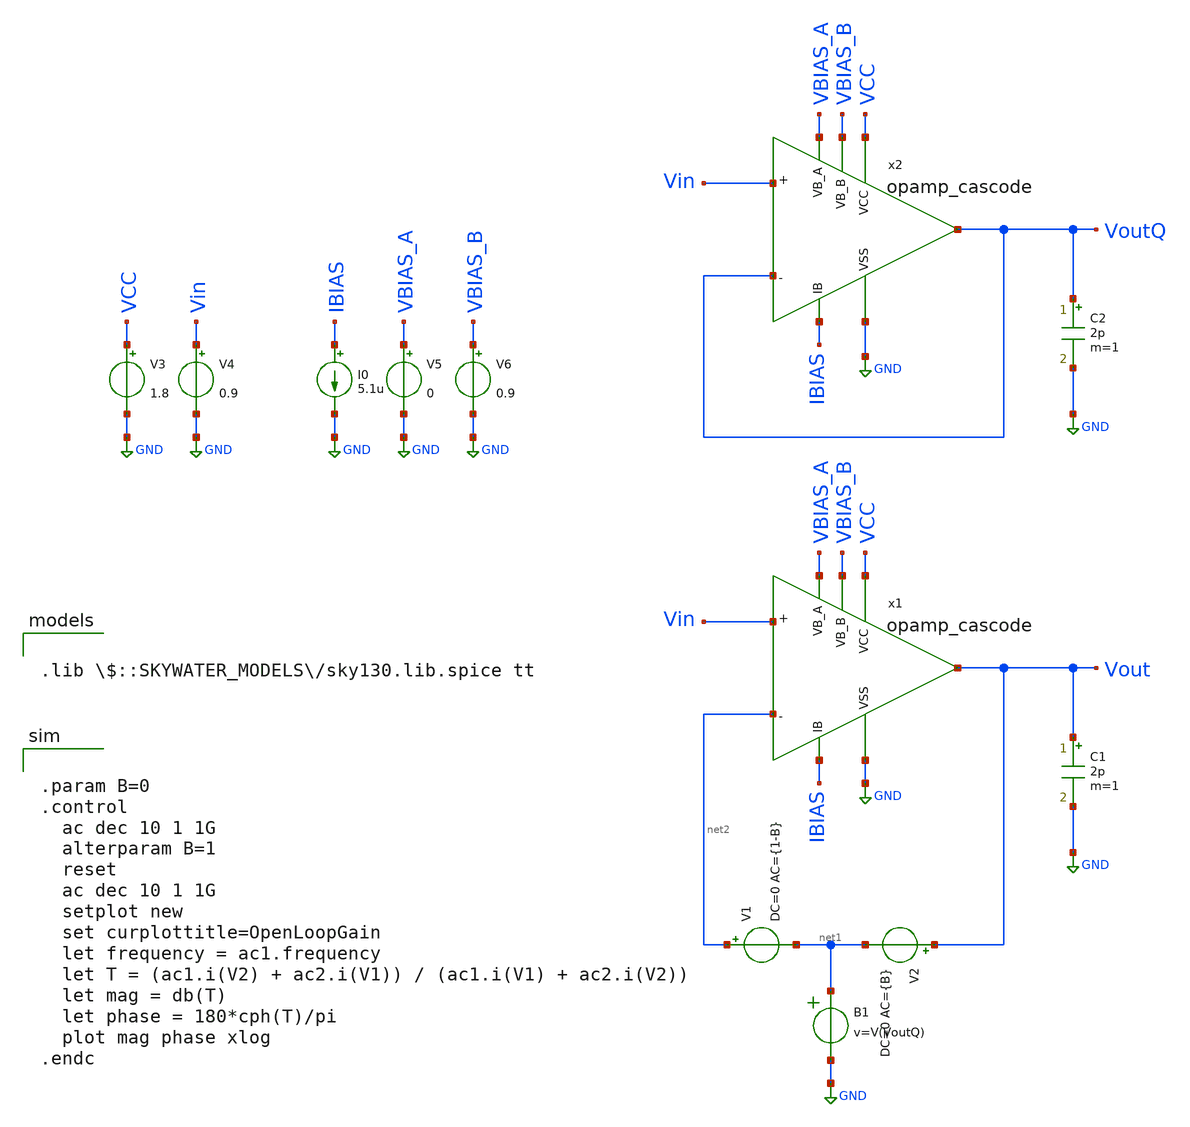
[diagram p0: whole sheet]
** sch_path: opamp_cascode_ac_ochoa.sch
**.subckt opamp_cascode_ac_ochoa
V3 VCC GND 1.8
V4 Vin GND 0.9
V2 Vout net1 DC=0 AC={B}
C1 Vout GND 2p m=1
C2 VoutQ GND 2p m=1
V1 net2 net1 DC=0 AC={1-B}
B1 net1 GND v=V(VoutQ)
V5 VBIAS_A GND 0
V6 VBIAS_B GND 0.9
I0 IBIAS GND 5.1u
x1 VCC GND VBIAS_B Vin net2 Vout IBIAS VBIAS_A opamp_cascode
x2 VCC GND VBIAS_B Vin VoutQ VoutQ IBIAS VBIAS_A opamp_cascode
**** begin user architecture code


.param B=0
.control
  ac dec 10 1 1G
  alterparam B=1
  reset
  ac dec 10 1 1G
  setplot new
  set curplottitle=OpenLoopGain
  let frequency = ac1.frequency
  let T = (ac1.i(V2) + ac2.i(V1)) / (ac1.i(V1) + ac2.i(V2))
  let mag = db(T)
  let phase = 180*cph(T)/pi
  plot mag phase xlog
.endc



.lib $::SKYWATER_MODELS/sky130.lib.spice tt

**** end user architecture code
**.ends

* expanding   symbol:  /home/zwierzak/projects/SKY130_OpAmp_GIT/opamp_cascode.sym # of pins=8
** sym_path: 03_Layout/opamp_cascode.sym
** sch_path: 03_Layout/opamp_cascode.sch
.subckt opamp_cascode VCC VSS VB_B IN_P IN_M OUT IB VB_A
*.ipin IN_P
*.ipin IN_M
*.ipin VCC
*.ipin VSS
*.opin OUT
*.ipin VB_A
*.ipin VB_B
*.ipin IB
XM100_3 IB IB VCC VCC sky130_fd_pr__pfet_01v8 L=3 W=5 nf=1 ad='int((nf+1)/2) * W/nf * 0.29' as='int((nf+2)/2) * W/nf * 0.29'
+ pd='2*int((nf+1)/2) * (W/nf + 0.29)' ps='2*int((nf+2)/2) * (W/nf + 0.29)' nrd='0.29 / W' nrs='0.29 / W'
+ sa=0 sb=0 sd=0 mult=2 m=2
XM10 OUT VB_A m9m10 VCC sky130_fd_pr__pfet_01v8 L=5 W=5 nf=1 ad='int((nf+1)/2) * W/nf * 0.29' as='int((nf+2)/2) * W/nf * 0.29'
+ pd='2*int((nf+1)/2) * (W/nf + 0.29)' ps='2*int((nf+2)/2) * (W/nf + 0.29)' nrd='0.29 / W' nrs='0.29 / W'
+ sa=0 sb=0 sd=0 mult=15 m=15
XM2 bias1 VB_A m1m2 VCC sky130_fd_pr__pfet_01v8 L=5 W=5 nf=1 ad='int((nf+1)/2) * W/nf * 0.29' as='int((nf+2)/2) * W/nf * 0.29'
+ pd='2*int((nf+1)/2) * (W/nf + 0.29)' ps='2*int((nf+2)/2) * (W/nf + 0.29)' nrd='0.29 / W' nrs='0.29 / W'
+ sa=0 sb=0 sd=0 mult=15 m=15
XM5 bias3 IN_M m100m5 VCC sky130_fd_pr__pfet_01v8 L=0.18 W=5 nf=1 ad='int((nf+1)/2) * W/nf * 0.29' as='int((nf+2)/2) * W/nf * 0.29'
+ pd='2*int((nf+1)/2) * (W/nf + 0.29)' ps='2*int((nf+2)/2) * (W/nf + 0.29)' nrd='0.29 / W' nrs='0.29 / W'
+ sa=0 sb=0 sd=0 mult=15 m=15
XM7 bias21 IN_P m100m5 VCC sky130_fd_pr__pfet_01v8 L=0.18 W=5 nf=1 ad='int((nf+1)/2) * W/nf * 0.29' as='int((nf+2)/2) * W/nf * 0.29'
+ pd='2*int((nf+1)/2) * (W/nf + 0.29)' ps='2*int((nf+2)/2) * (W/nf + 0.29)' nrd='0.29 / W' nrs='0.29 / W'
+ sa=0 sb=0 sd=0 mult=15 m=15
XM6 bias3 bias3 VSS VSS sky130_fd_pr__nfet_01v8 L=1 W=1.25 nf=1 ad='int((nf+1)/2) * W/nf * 0.29' as='int((nf+2)/2) * W/nf * 0.29'
+ pd='2*int((nf+1)/2) * (W/nf + 0.29)' ps='2*int((nf+2)/2) * (W/nf + 0.29)' nrd='0.29 / W' nrs='0.29 / W'
+ sa=0 sb=0 sd=0 mult=1 m=1
XM8 bias21 bias21 VSS VSS sky130_fd_pr__nfet_01v8 L=1 W=1.25 nf=1 ad='int((nf+1)/2) * W/nf * 0.29' as='int((nf+2)/2) * W/nf * 0.29'
+ pd='2*int((nf+1)/2) * (W/nf + 0.29)' ps='2*int((nf+2)/2) * (W/nf + 0.29)' nrd='0.29 / W' nrs='0.29 / W'
+ sa=0 sb=0 sd=0 mult=1 m=1
XM12 m11m12 bias21 VSS VSS sky130_fd_pr__nfet_01v8 L=1 W=5 nf=1 ad='int((nf+1)/2) * W/nf * 0.29' as='int((nf+2)/2) * W/nf * 0.29'
+ pd='2*int((nf+1)/2) * (W/nf + 0.29)' ps='2*int((nf+2)/2) * (W/nf + 0.29)' nrd='0.29 / W' nrs='0.29 / W'
+ sa=0 sb=0 sd=0 mult=1 m=1
XM11 OUT VB_B m11m12 VSS sky130_fd_pr__nfet_01v8 L=5 W=5 nf=1 ad='int((nf+1)/2) * W/nf * 0.29' as='int((nf+2)/2) * W/nf * 0.29'
+ pd='2*int((nf+1)/2) * (W/nf + 0.29)' ps='2*int((nf+2)/2) * (W/nf + 0.29)' nrd='0.29 / W' nrs='0.29 / W'
+ sa=0 sb=0 sd=0 mult=15 m=15
XM3 bias1 VB_B m3m4 VSS sky130_fd_pr__nfet_01v8 L=5 W=5 nf=1 ad='int((nf+1)/2) * W/nf * 0.29' as='int((nf+2)/2) * W/nf * 0.29'
+ pd='2*int((nf+1)/2) * (W/nf + 0.29)' ps='2*int((nf+2)/2) * (W/nf + 0.29)' nrd='0.29 / W' nrs='0.29 / W'
+ sa=0 sb=0 sd=0 mult=15 m=15
XM100_1 m100m5 IB VCC VCC sky130_fd_pr__pfet_01v8 L=3 W=5 nf=1 ad='int((nf+1)/2) * W/nf * 0.29' as='int((nf+2)/2) * W/nf * 0.29'
+ pd='2*int((nf+1)/2) * (W/nf + 0.29)' ps='2*int((nf+2)/2) * (W/nf + 0.29)' nrd='0.29 / W' nrs='0.29 / W'
+ sa=0 sb=0 sd=0 mult=3 m=3
XM5_1 bias3 IN_M m100m5 VCC sky130_fd_pr__pfet_01v8 L=0.18 W=5 nf=1 ad='int((nf+1)/2) * W/nf * 0.29'
+ as='int((nf+2)/2) * W/nf * 0.29' pd='2*int((nf+1)/2) * (W/nf + 0.29)' ps='2*int((nf+2)/2) * (W/nf + 0.29)'
+ nrd='0.29 / W' nrs='0.29 / W' sa=0 sb=0 sd=0 mult=15 m=15
XM7_1 bias21 IN_P m100m5 VCC sky130_fd_pr__pfet_01v8 L=0.18 W=5 nf=1 ad='int((nf+1)/2) * W/nf * 0.29'
+ as='int((nf+2)/2) * W/nf * 0.29' pd='2*int((nf+1)/2) * (W/nf + 0.29)' ps='2*int((nf+2)/2) * (W/nf + 0.29)'
+ nrd='0.29 / W' nrs='0.29 / W' sa=0 sb=0 sd=0 mult=15 m=15
XM9 m9m10 bias1 VCC VCC sky130_fd_pr__pfet_01v8 L=15 W=5 nf=1 ad='int((nf+1)/2) * W/nf * 0.29' as='int((nf+2)/2) * W/nf * 0.29'
+ pd='2*int((nf+1)/2) * (W/nf + 0.29)' ps='2*int((nf+2)/2) * (W/nf + 0.29)' nrd='0.29 / W' nrs='0.29 / W'
+ sa=0 sb=0 sd=0 mult=100 m=100
XM9_1 m9m10 bias1 VCC VCC sky130_fd_pr__pfet_01v8 L=15 W=5 nf=1 ad='int((nf+1)/2) * W/nf * 0.29' as='int((nf+2)/2) * W/nf * 0.29'
+ pd='2*int((nf+1)/2) * (W/nf + 0.29)' ps='2*int((nf+2)/2) * (W/nf + 0.29)' nrd='0.29 / W' nrs='0.29 / W'
+ sa=0 sb=0 sd=0 mult=100 m=100
XM9_2 m9m10 bias1 VCC VCC sky130_fd_pr__pfet_01v8 L=15 W=5 nf=1 ad='int((nf+1)/2) * W/nf * 0.29' as='int((nf+2)/2) * W/nf * 0.29'
+ pd='2*int((nf+1)/2) * (W/nf + 0.29)' ps='2*int((nf+2)/2) * (W/nf + 0.29)' nrd='0.29 / W' nrs='0.29 / W'
+ sa=0 sb=0 sd=0 mult=100 m=100
XM9_3 m9m10 bias1 VCC VCC sky130_fd_pr__pfet_01v8 L=15 W=5 nf=1 ad='int((nf+1)/2) * W/nf * 0.29' as='int((nf+2)/2) * W/nf * 0.29'
+ pd='2*int((nf+1)/2) * (W/nf + 0.29)' ps='2*int((nf+2)/2) * (W/nf + 0.29)' nrd='0.29 / W' nrs='0.29 / W'
+ sa=0 sb=0 sd=0 mult=100 m=100
XM9_4 m9m10 bias1 VCC VCC sky130_fd_pr__pfet_01v8 L=15 W=5 nf=1 ad='int((nf+1)/2) * W/nf * 0.29' as='int((nf+2)/2) * W/nf * 0.29'
+ pd='2*int((nf+1)/2) * (W/nf + 0.29)' ps='2*int((nf+2)/2) * (W/nf + 0.29)' nrd='0.29 / W' nrs='0.29 / W'
+ sa=0 sb=0 sd=0 mult=100 m=100
XM1 m1m2 bias1 VCC VCC sky130_fd_pr__pfet_01v8 L=15 W=5 nf=1 ad='int((nf+1)/2) * W/nf * 0.29' as='int((nf+2)/2) * W/nf * 0.29'
+ pd='2*int((nf+1)/2) * (W/nf + 0.29)' ps='2*int((nf+2)/2) * (W/nf + 0.29)' nrd='0.29 / W' nrs='0.29 / W'
+ sa=0 sb=0 sd=0 mult=100 m=100
XM1_1 m1m2 bias1 VCC VCC sky130_fd_pr__pfet_01v8 L=15 W=5 nf=1 ad='int((nf+1)/2) * W/nf * 0.29' as='int((nf+2)/2) * W/nf * 0.29'
+ pd='2*int((nf+1)/2) * (W/nf + 0.29)' ps='2*int((nf+2)/2) * (W/nf + 0.29)' nrd='0.29 / W' nrs='0.29 / W'
+ sa=0 sb=0 sd=0 mult=100 m=100
XM1_2 m1m2 bias1 VCC VCC sky130_fd_pr__pfet_01v8 L=15 W=5 nf=1 ad='int((nf+1)/2) * W/nf * 0.29' as='int((nf+2)/2) * W/nf * 0.29'
+ pd='2*int((nf+1)/2) * (W/nf + 0.29)' ps='2*int((nf+2)/2) * (W/nf + 0.29)' nrd='0.29 / W' nrs='0.29 / W'
+ sa=0 sb=0 sd=0 mult=100 m=100
XM1_3 m1m2 bias1 VCC VCC sky130_fd_pr__pfet_01v8 L=15 W=5 nf=1 ad='int((nf+1)/2) * W/nf * 0.29' as='int((nf+2)/2) * W/nf * 0.29'
+ pd='2*int((nf+1)/2) * (W/nf + 0.29)' ps='2*int((nf+2)/2) * (W/nf + 0.29)' nrd='0.29 / W' nrs='0.29 / W'
+ sa=0 sb=0 sd=0 mult=100 m=100
XM1_4 m1m2 bias1 VCC VCC sky130_fd_pr__pfet_01v8 L=15 W=5 nf=1 ad='int((nf+1)/2) * W/nf * 0.29' as='int((nf+2)/2) * W/nf * 0.29'
+ pd='2*int((nf+1)/2) * (W/nf + 0.29)' ps='2*int((nf+2)/2) * (W/nf + 0.29)' nrd='0.29 / W' nrs='0.29 / W'
+ sa=0 sb=0 sd=0 mult=100 m=100
XM100_2 m100m5 IB VCC VCC sky130_fd_pr__pfet_01v8 L=3 W=5 nf=1 ad='int((nf+1)/2) * W/nf * 0.29' as='int((nf+2)/2) * W/nf * 0.29'
+ pd='2*int((nf+1)/2) * (W/nf + 0.29)' ps='2*int((nf+2)/2) * (W/nf + 0.29)' nrd='0.29 / W' nrs='0.29 / W'
+ sa=0 sb=0 sd=0 mult=3 m=3
XM10_1 OUT VB_A m9m10 VCC sky130_fd_pr__pfet_01v8 L=5 W=5 nf=1 ad='int((nf+1)/2) * W/nf * 0.29' as='int((nf+2)/2) * W/nf * 0.29'
+ pd='2*int((nf+1)/2) * (W/nf + 0.29)' ps='2*int((nf+2)/2) * (W/nf + 0.29)' nrd='0.29 / W' nrs='0.29 / W'
+ sa=0 sb=0 sd=0 mult=15 m=15
XM2_1 bias1 VB_A m1m2 VCC sky130_fd_pr__pfet_01v8 L=5 W=5 nf=1 ad='int((nf+1)/2) * W/nf * 0.29' as='int((nf+2)/2) * W/nf * 0.29'
+ pd='2*int((nf+1)/2) * (W/nf + 0.29)' ps='2*int((nf+2)/2) * (W/nf + 0.29)' nrd='0.29 / W' nrs='0.29 / W'
+ sa=0 sb=0 sd=0 mult=15 m=15
XM3_1 bias1 VB_B m3m4 VSS sky130_fd_pr__nfet_01v8 L=5 W=5 nf=1 ad='int((nf+1)/2) * W/nf * 0.29' as='int((nf+2)/2) * W/nf * 0.29'
+ pd='2*int((nf+1)/2) * (W/nf + 0.29)' ps='2*int((nf+2)/2) * (W/nf + 0.29)' nrd='0.29 / W' nrs='0.29 / W'
+ sa=0 sb=0 sd=0 mult=15 m=15
XM11_1 OUT VB_B m11m12 VSS sky130_fd_pr__nfet_01v8 L=5 W=5 nf=1 ad='int((nf+1)/2) * W/nf * 0.29' as='int((nf+2)/2) * W/nf * 0.29'
+ pd='2*int((nf+1)/2) * (W/nf + 0.29)' ps='2*int((nf+2)/2) * (W/nf + 0.29)' nrd='0.29 / W' nrs='0.29 / W'
+ sa=0 sb=0 sd=0 mult=15 m=15
XM4 m3m4 bias3 VSS VSS sky130_fd_pr__nfet_01v8 L=1 W=5 nf=1 ad='int((nf+1)/2) * W/nf * 0.29' as='int((nf+2)/2) * W/nf * 0.29'
+ pd='2*int((nf+1)/2) * (W/nf + 0.29)' ps='2*int((nf+2)/2) * (W/nf + 0.29)' nrd='0.29 / W' nrs='0.29 / W'
+ sa=0 sb=0 sd=0 mult=1 m=1
XM6_1 bias3 bias3 VSS VSS sky130_fd_pr__nfet_01v8 L=1 W=1.25 nf=1 ad='int((nf+1)/2) * W/nf * 0.29' as='int((nf+2)/2) * W/nf * 0.29'
+ pd='2*int((nf+1)/2) * (W/nf + 0.29)' ps='2*int((nf+2)/2) * (W/nf + 0.29)' nrd='0.29 / W' nrs='0.29 / W'
+ sa=0 sb=0 sd=0 mult=1 m=1
XM8_1 bias21 bias21 VSS VSS sky130_fd_pr__nfet_01v8 L=1 W=1.25 nf=1 ad='int((nf+1)/2) * W/nf * 0.29'
+ as='int((nf+2)/2) * W/nf * 0.29' pd='2*int((nf+1)/2) * (W/nf + 0.29)' ps='2*int((nf+2)/2) * (W/nf + 0.29)'
+ nrd='0.29 / W' nrs='0.29 / W' sa=0 sb=0 sd=0 mult=1 m=1
XM6_2 bias3 bias3 VSS VSS sky130_fd_pr__nfet_01v8 L=1 W=1.25 nf=1 ad='int((nf+1)/2) * W/nf * 0.29' as='int((nf+2)/2) * W/nf * 0.29'
+ pd='2*int((nf+1)/2) * (W/nf + 0.29)' ps='2*int((nf+2)/2) * (W/nf + 0.29)' nrd='0.29 / W' nrs='0.29 / W'
+ sa=0 sb=0 sd=0 mult=1 m=1
XM6_3 bias3 bias3 VSS VSS sky130_fd_pr__nfet_01v8 L=1 W=1.25 nf=1 ad='int((nf+1)/2) * W/nf * 0.29' as='int((nf+2)/2) * W/nf * 0.29'
+ pd='2*int((nf+1)/2) * (W/nf + 0.29)' ps='2*int((nf+2)/2) * (W/nf + 0.29)' nrd='0.29 / W' nrs='0.29 / W'
+ sa=0 sb=0 sd=0 mult=1 m=1
XM9_dummy_1 dummy_9 bias1 dummy_9 VCC sky130_fd_pr__pfet_01v8 L=15 W=5 nf=1 ad='int((nf+1)/2) * W/nf * 0.29'
+ as='int((nf+2)/2) * W/nf * 0.29' pd='2*int((nf+1)/2) * (W/nf + 0.29)' ps='2*int((nf+2)/2) * (W/nf + 0.29)'
+ nrd='0.29 / W' nrs='0.29 / W' sa=0 sb=0 sd=0 mult=102 m=102
XM9_dummy_2 dummy_9 bias1 dummy_9 VCC sky130_fd_pr__pfet_01v8 L=15 W=5 nf=1 ad='int((nf+1)/2) * W/nf * 0.29'
+ as='int((nf+2)/2) * W/nf * 0.29' pd='2*int((nf+1)/2) * (W/nf + 0.29)' ps='2*int((nf+2)/2) * (W/nf + 0.29)'
+ nrd='0.29 / W' nrs='0.29 / W' sa=0 sb=0 sd=0 mult=102 m=102
XM9_dummy_3 dummy_9 bias1 dummy_9 VCC sky130_fd_pr__pfet_01v8 L=15 W=5 nf=1 ad='int((nf+1)/2) * W/nf * 0.29'
+ as='int((nf+2)/2) * W/nf * 0.29' pd='2*int((nf+1)/2) * (W/nf + 0.29)' ps='2*int((nf+2)/2) * (W/nf + 0.29)'
+ nrd='0.29 / W' nrs='0.29 / W' sa=0 sb=0 sd=0 mult=1 m=1
XM9_dummy_4 dummy_9 bias1 dummy_9 VCC sky130_fd_pr__pfet_01v8 L=15 W=5 nf=1 ad='int((nf+1)/2) * W/nf * 0.29'
+ as='int((nf+2)/2) * W/nf * 0.29' pd='2*int((nf+1)/2) * (W/nf + 0.29)' ps='2*int((nf+2)/2) * (W/nf + 0.29)'
+ nrd='0.29 / W' nrs='0.29 / W' sa=0 sb=0 sd=0 mult=1 m=1
XM9_dummy_5 dummy_9 bias1 dummy_9 VCC sky130_fd_pr__pfet_01v8 L=15 W=5 nf=1 ad='int((nf+1)/2) * W/nf * 0.29'
+ as='int((nf+2)/2) * W/nf * 0.29' pd='2*int((nf+1)/2) * (W/nf + 0.29)' ps='2*int((nf+2)/2) * (W/nf + 0.29)'
+ nrd='0.29 / W' nrs='0.29 / W' sa=0 sb=0 sd=0 mult=1 m=1
XM9_dummy_6 dummy_9 bias1 dummy_9 VCC sky130_fd_pr__pfet_01v8 L=15 W=5 nf=1 ad='int((nf+1)/2) * W/nf * 0.29'
+ as='int((nf+2)/2) * W/nf * 0.29' pd='2*int((nf+1)/2) * (W/nf + 0.29)' ps='2*int((nf+2)/2) * (W/nf + 0.29)'
+ nrd='0.29 / W' nrs='0.29 / W' sa=0 sb=0 sd=0 mult=1 m=1
XM9_dummy_7 dummy_9 bias1 dummy_9 VCC sky130_fd_pr__pfet_01v8 L=15 W=5 nf=1 ad='int((nf+1)/2) * W/nf * 0.29'
+ as='int((nf+2)/2) * W/nf * 0.29' pd='2*int((nf+1)/2) * (W/nf + 0.29)' ps='2*int((nf+2)/2) * (W/nf + 0.29)'
+ nrd='0.29 / W' nrs='0.29 / W' sa=0 sb=0 sd=0 mult=1 m=1
XM9_dummy_8 dummy_9 bias1 dummy_9 VCC sky130_fd_pr__pfet_01v8 L=15 W=5 nf=1 ad='int((nf+1)/2) * W/nf * 0.29'
+ as='int((nf+2)/2) * W/nf * 0.29' pd='2*int((nf+1)/2) * (W/nf + 0.29)' ps='2*int((nf+2)/2) * (W/nf + 0.29)'
+ nrd='0.29 / W' nrs='0.29 / W' sa=0 sb=0 sd=0 mult=1 m=1
XM9_dummy_9 dummy_9 bias1 dummy_9 VCC sky130_fd_pr__pfet_01v8 L=15 W=5 nf=1 ad='int((nf+1)/2) * W/nf * 0.29'
+ as='int((nf+2)/2) * W/nf * 0.29' pd='2*int((nf+1)/2) * (W/nf + 0.29)' ps='2*int((nf+2)/2) * (W/nf + 0.29)'
+ nrd='0.29 / W' nrs='0.29 / W' sa=0 sb=0 sd=0 mult=1 m=1
XM9_dummy_10 dummy_9 bias1 dummy_9 VCC sky130_fd_pr__pfet_01v8 L=15 W=5 nf=1 ad='int((nf+1)/2) * W/nf * 0.29'
+ as='int((nf+2)/2) * W/nf * 0.29' pd='2*int((nf+1)/2) * (W/nf + 0.29)' ps='2*int((nf+2)/2) * (W/nf + 0.29)'
+ nrd='0.29 / W' nrs='0.29 / W' sa=0 sb=0 sd=0 mult=1 m=1
XM9_dummy_11 dummy_9 bias1 dummy_9 VCC sky130_fd_pr__pfet_01v8 L=15 W=5 nf=1 ad='int((nf+1)/2) * W/nf * 0.29'
+ as='int((nf+2)/2) * W/nf * 0.29' pd='2*int((nf+1)/2) * (W/nf + 0.29)' ps='2*int((nf+2)/2) * (W/nf + 0.29)'
+ nrd='0.29 / W' nrs='0.29 / W' sa=0 sb=0 sd=0 mult=1 m=1
XM9_dummy_12 dummy_9 bias1 dummy_9 VCC sky130_fd_pr__pfet_01v8 L=15 W=5 nf=1 ad='int((nf+1)/2) * W/nf * 0.29'
+ as='int((nf+2)/2) * W/nf * 0.29' pd='2*int((nf+1)/2) * (W/nf + 0.29)' ps='2*int((nf+2)/2) * (W/nf + 0.29)'
+ nrd='0.29 / W' nrs='0.29 / W' sa=0 sb=0 sd=0 mult=1 m=1
XM100_dummy_1 dummy_100 IB dummy_100 VCC sky130_fd_pr__pfet_01v8 L=3 W=5 nf=1 ad='int((nf+1)/2) * W/nf * 0.29'
+ as='int((nf+2)/2) * W/nf * 0.29' pd='2*int((nf+1)/2) * (W/nf + 0.29)' ps='2*int((nf+2)/2) * (W/nf + 0.29)'
+ nrd='0.29 / W' nrs='0.29 / W' sa=0 sb=0 sd=0 mult=5 m=5
XM100_dummy_2 dummy_100 IB dummy_100 VCC sky130_fd_pr__pfet_01v8 L=3 W=5 nf=1 ad='int((nf+1)/2) * W/nf * 0.29'
+ as='int((nf+2)/2) * W/nf * 0.29' pd='2*int((nf+1)/2) * (W/nf + 0.29)' ps='2*int((nf+2)/2) * (W/nf + 0.29)'
+ nrd='0.29 / W' nrs='0.29 / W' sa=0 sb=0 sd=0 mult=5 m=5
XM100_dummy_3 dummy_100 IB dummy_100 VCC sky130_fd_pr__pfet_01v8 L=3 W=5 nf=1 ad='int((nf+1)/2) * W/nf * 0.29'
+ as='int((nf+2)/2) * W/nf * 0.29' pd='2*int((nf+1)/2) * (W/nf + 0.29)' ps='2*int((nf+2)/2) * (W/nf + 0.29)'
+ nrd='0.29 / W' nrs='0.29 / W' sa=0 sb=0 sd=0 mult=2 m=2
XM100_dummy_4 dummy_100 IB dummy_100 VCC sky130_fd_pr__pfet_01v8 L=3 W=5 nf=1 ad='int((nf+1)/2) * W/nf * 0.29'
+ as='int((nf+2)/2) * W/nf * 0.29' pd='2*int((nf+1)/2) * (W/nf + 0.29)' ps='2*int((nf+2)/2) * (W/nf + 0.29)'
+ nrd='0.29 / W' nrs='0.29 / W' sa=0 sb=0 sd=0 mult=2 m=2
XM100_dummy_5 dummy_100 IB dummy_100 VCC sky130_fd_pr__pfet_01v8 L=3 W=5 nf=1 ad='int((nf+1)/2) * W/nf * 0.29'
+ as='int((nf+2)/2) * W/nf * 0.29' pd='2*int((nf+1)/2) * (W/nf + 0.29)' ps='2*int((nf+2)/2) * (W/nf + 0.29)'
+ nrd='0.29 / W' nrs='0.29 / W' sa=0 sb=0 sd=0 mult=1 m=1
XM100_dummy_6 dummy_100 IB dummy_100 VCC sky130_fd_pr__pfet_01v8 L=3 W=5 nf=1 ad='int((nf+1)/2) * W/nf * 0.29'
+ as='int((nf+2)/2) * W/nf * 0.29' pd='2*int((nf+1)/2) * (W/nf + 0.29)' ps='2*int((nf+2)/2) * (W/nf + 0.29)'
+ nrd='0.29 / W' nrs='0.29 / W' sa=0 sb=0 sd=0 mult=1 m=1
XM100_dummy_7 dummy_100 IB dummy_100 VCC sky130_fd_pr__pfet_01v8 L=3 W=5 nf=1 ad='int((nf+1)/2) * W/nf * 0.29'
+ as='int((nf+2)/2) * W/nf * 0.29' pd='2*int((nf+1)/2) * (W/nf + 0.29)' ps='2*int((nf+2)/2) * (W/nf + 0.29)'
+ nrd='0.29 / W' nrs='0.29 / W' sa=0 sb=0 sd=0 mult=1 m=1
XM100_dummy_8 dummy_100 IB dummy_100 VCC sky130_fd_pr__pfet_01v8 L=3 W=5 nf=1 ad='int((nf+1)/2) * W/nf * 0.29'
+ as='int((nf+2)/2) * W/nf * 0.29' pd='2*int((nf+1)/2) * (W/nf + 0.29)' ps='2*int((nf+2)/2) * (W/nf + 0.29)'
+ nrd='0.29 / W' nrs='0.29 / W' sa=0 sb=0 sd=0 mult=1 m=1
XM100_dummy_9 dummy_100 IB dummy_100 VCC sky130_fd_pr__pfet_01v8 L=3 W=5 nf=1 ad='int((nf+1)/2) * W/nf * 0.29'
+ as='int((nf+2)/2) * W/nf * 0.29' pd='2*int((nf+1)/2) * (W/nf + 0.29)' ps='2*int((nf+2)/2) * (W/nf + 0.29)'
+ nrd='0.29 / W' nrs='0.29 / W' sa=0 sb=0 sd=0 mult=1 m=1
XM100_dummy_10 dummy_100 IB dummy_100 VCC sky130_fd_pr__pfet_01v8 L=3 W=5 nf=1 ad='int((nf+1)/2) * W/nf * 0.29'
+ as='int((nf+2)/2) * W/nf * 0.29' pd='2*int((nf+1)/2) * (W/nf + 0.29)' ps='2*int((nf+2)/2) * (W/nf + 0.29)'
+ nrd='0.29 / W' nrs='0.29 / W' sa=0 sb=0 sd=0 mult=1 m=1
XM2_dummy_1 dummy_2 VB_A dummy_2 VCC sky130_fd_pr__pfet_01v8 L=5 W=5 nf=1 ad='int((nf+1)/2) * W/nf * 0.29'
+ as='int((nf+2)/2) * W/nf * 0.29' pd='2*int((nf+1)/2) * (W/nf + 0.29)' ps='2*int((nf+2)/2) * (W/nf + 0.29)'
+ nrd='0.29 / W' nrs='0.29 / W' sa=0 sb=0 sd=0 mult=17 m=17
XM2_dummy_2 dummy_2 VB_A dummy_2 VCC sky130_fd_pr__pfet_01v8 L=5 W=5 nf=1 ad='int((nf+1)/2) * W/nf * 0.29'
+ as='int((nf+2)/2) * W/nf * 0.29' pd='2*int((nf+1)/2) * (W/nf + 0.29)' ps='2*int((nf+2)/2) * (W/nf + 0.29)'
+ nrd='0.29 / W' nrs='0.29 / W' sa=0 sb=0 sd=0 mult=17 m=17
XM2_dummy_3 dummy_2 VB_A dummy_2 VCC sky130_fd_pr__pfet_01v8 L=5 W=5 nf=1 ad='int((nf+1)/2) * W/nf * 0.29'
+ as='int((nf+2)/2) * W/nf * 0.29' pd='2*int((nf+1)/2) * (W/nf + 0.29)' ps='2*int((nf+2)/2) * (W/nf + 0.29)'
+ nrd='0.29 / W' nrs='0.29 / W' sa=0 sb=0 sd=0 mult=1 m=1
XM2_dummy_4 dummy_2 VB_A dummy_2 VCC sky130_fd_pr__pfet_01v8 L=5 W=5 nf=1 ad='int((nf+1)/2) * W/nf * 0.29'
+ as='int((nf+2)/2) * W/nf * 0.29' pd='2*int((nf+1)/2) * (W/nf + 0.29)' ps='2*int((nf+2)/2) * (W/nf + 0.29)'
+ nrd='0.29 / W' nrs='0.29 / W' sa=0 sb=0 sd=0 mult=1 m=1
XM2_dummy_5 dummy_2 VB_A dummy_2 VCC sky130_fd_pr__pfet_01v8 L=5 W=5 nf=1 ad='int((nf+1)/2) * W/nf * 0.29'
+ as='int((nf+2)/2) * W/nf * 0.29' pd='2*int((nf+1)/2) * (W/nf + 0.29)' ps='2*int((nf+2)/2) * (W/nf + 0.29)'
+ nrd='0.29 / W' nrs='0.29 / W' sa=0 sb=0 sd=0 mult=1 m=1
XM2_dummy_6 dummy_2 VB_A dummy_2 VCC sky130_fd_pr__pfet_01v8 L=5 W=5 nf=1 ad='int((nf+1)/2) * W/nf * 0.29'
+ as='int((nf+2)/2) * W/nf * 0.29' pd='2*int((nf+1)/2) * (W/nf + 0.29)' ps='2*int((nf+2)/2) * (W/nf + 0.29)'
+ nrd='0.29 / W' nrs='0.29 / W' sa=0 sb=0 sd=0 mult=1 m=1
XM2_dummy_7 dummy_2 VB_A dummy_2 VCC sky130_fd_pr__pfet_01v8 L=5 W=5 nf=1 ad='int((nf+1)/2) * W/nf * 0.29'
+ as='int((nf+2)/2) * W/nf * 0.29' pd='2*int((nf+1)/2) * (W/nf + 0.29)' ps='2*int((nf+2)/2) * (W/nf + 0.29)'
+ nrd='0.29 / W' nrs='0.29 / W' sa=0 sb=0 sd=0 mult=1 m=1
XM2_dummy_8 dummy_2 VB_A dummy_2 VCC sky130_fd_pr__pfet_01v8 L=5 W=5 nf=1 ad='int((nf+1)/2) * W/nf * 0.29'
+ as='int((nf+2)/2) * W/nf * 0.29' pd='2*int((nf+1)/2) * (W/nf + 0.29)' ps='2*int((nf+2)/2) * (W/nf + 0.29)'
+ nrd='0.29 / W' nrs='0.29 / W' sa=0 sb=0 sd=0 mult=1 m=1
XM2_dummy_9 dummy_2 VB_A dummy_2 VCC sky130_fd_pr__pfet_01v8 L=5 W=5 nf=1 ad='int((nf+1)/2) * W/nf * 0.29'
+ as='int((nf+2)/2) * W/nf * 0.29' pd='2*int((nf+1)/2) * (W/nf + 0.29)' ps='2*int((nf+2)/2) * (W/nf + 0.29)'
+ nrd='0.29 / W' nrs='0.29 / W' sa=0 sb=0 sd=0 mult=1 m=1
XM2_dummy_10 dummy_2 VB_A dummy_2 VCC sky130_fd_pr__pfet_01v8 L=5 W=5 nf=1 ad='int((nf+1)/2) * W/nf * 0.29'
+ as='int((nf+2)/2) * W/nf * 0.29' pd='2*int((nf+1)/2) * (W/nf + 0.29)' ps='2*int((nf+2)/2) * (W/nf + 0.29)'
+ nrd='0.29 / W' nrs='0.29 / W' sa=0 sb=0 sd=0 mult=1 m=1
XM4_dummy_1 dummy_4 bias3 dummy_4 VSS sky130_fd_pr__nfet_01v8 L=1 W=1.25 nf=1 ad='int((nf+1)/2) * W/nf * 0.29'
+ as='int((nf+2)/2) * W/nf * 0.29' pd='2*int((nf+1)/2) * (W/nf + 0.29)' ps='2*int((nf+2)/2) * (W/nf + 0.29)'
+ nrd='0.29 / W' nrs='0.29 / W' sa=0 sb=0 sd=0 mult=6 m=6
XM4_dummy_2 dummy_4 bias3 dummy_4 VSS sky130_fd_pr__nfet_01v8 L=1 W=1.25 nf=1 ad='int((nf+1)/2) * W/nf * 0.29'
+ as='int((nf+2)/2) * W/nf * 0.29' pd='2*int((nf+1)/2) * (W/nf + 0.29)' ps='2*int((nf+2)/2) * (W/nf + 0.29)'
+ nrd='0.29 / W' nrs='0.29 / W' sa=0 sb=0 sd=0 mult=6 m=6
XM4_dummy_3 dummy_4 bias3 dummy_4 VSS sky130_fd_pr__nfet_01v8 L=1 W=1.25 nf=1 ad='int((nf+1)/2) * W/nf * 0.29'
+ as='int((nf+2)/2) * W/nf * 0.29' pd='2*int((nf+1)/2) * (W/nf + 0.29)' ps='2*int((nf+2)/2) * (W/nf + 0.29)'
+ nrd='0.29 / W' nrs='0.29 / W' sa=0 sb=0 sd=0 mult=1 m=1
XM4_dummy_4 dummy_4 bias3 dummy_4 VSS sky130_fd_pr__nfet_01v8 L=1 W=1.25 nf=1 ad='int((nf+1)/2) * W/nf * 0.29'
+ as='int((nf+2)/2) * W/nf * 0.29' pd='2*int((nf+1)/2) * (W/nf + 0.29)' ps='2*int((nf+2)/2) * (W/nf + 0.29)'
+ nrd='0.29 / W' nrs='0.29 / W' sa=0 sb=0 sd=0 mult=1 m=1
XM4_dummy_5 dummy_4 bias3 dummy_4 VSS sky130_fd_pr__nfet_01v8 L=1 W=1.25 nf=1 ad='int((nf+1)/2) * W/nf * 0.29'
+ as='int((nf+2)/2) * W/nf * 0.29' pd='2*int((nf+1)/2) * (W/nf + 0.29)' ps='2*int((nf+2)/2) * (W/nf + 0.29)'
+ nrd='0.29 / W' nrs='0.29 / W' sa=0 sb=0 sd=0 mult=1 m=1
XM4_dummy_6 dummy_4 bias3 dummy_4 VSS sky130_fd_pr__nfet_01v8 L=1 W=1.25 nf=1 ad='int((nf+1)/2) * W/nf * 0.29'
+ as='int((nf+2)/2) * W/nf * 0.29' pd='2*int((nf+1)/2) * (W/nf + 0.29)' ps='2*int((nf+2)/2) * (W/nf + 0.29)'
+ nrd='0.29 / W' nrs='0.29 / W' sa=0 sb=0 sd=0 mult=1 m=1
XM4_dummy_7 dummy_4 bias3 dummy_4 VSS sky130_fd_pr__nfet_01v8 L=1 W=1.25 nf=1 ad='int((nf+1)/2) * W/nf * 0.29'
+ as='int((nf+2)/2) * W/nf * 0.29' pd='2*int((nf+1)/2) * (W/nf + 0.29)' ps='2*int((nf+2)/2) * (W/nf + 0.29)'
+ nrd='0.29 / W' nrs='0.29 / W' sa=0 sb=0 sd=0 mult=1 m=1
XM4_dummy_8 dummy_4 bias3 dummy_4 VSS sky130_fd_pr__nfet_01v8 L=1 W=1.25 nf=1 ad='int((nf+1)/2) * W/nf * 0.29'
+ as='int((nf+2)/2) * W/nf * 0.29' pd='2*int((nf+1)/2) * (W/nf + 0.29)' ps='2*int((nf+2)/2) * (W/nf + 0.29)'
+ nrd='0.29 / W' nrs='0.29 / W' sa=0 sb=0 sd=0 mult=1 m=1
XM4_dummy_9 dummy_4 bias3 dummy_4 VSS sky130_fd_pr__nfet_01v8 L=1 W=1.25 nf=1 ad='int((nf+1)/2) * W/nf * 0.29'
+ as='int((nf+2)/2) * W/nf * 0.29' pd='2*int((nf+1)/2) * (W/nf + 0.29)' ps='2*int((nf+2)/2) * (W/nf + 0.29)'
+ nrd='0.29 / W' nrs='0.29 / W' sa=0 sb=0 sd=0 mult=1 m=1
XM4_dummy_10 dummy_4 bias3 dummy_4 VSS sky130_fd_pr__nfet_01v8 L=1 W=1.25 nf=1 ad='int((nf+1)/2) * W/nf * 0.29'
+ as='int((nf+2)/2) * W/nf * 0.29' pd='2*int((nf+1)/2) * (W/nf + 0.29)' ps='2*int((nf+2)/2) * (W/nf + 0.29)'
+ nrd='0.29 / W' nrs='0.29 / W' sa=0 sb=0 sd=0 mult=1 m=1
XM8_2 bias21 bias21 VSS VSS sky130_fd_pr__nfet_01v8 L=1 W=1.25 nf=1 ad='int((nf+1)/2) * W/nf * 0.29'
+ as='int((nf+2)/2) * W/nf * 0.29' pd='2*int((nf+1)/2) * (W/nf + 0.29)' ps='2*int((nf+2)/2) * (W/nf + 0.29)'
+ nrd='0.29 / W' nrs='0.29 / W' sa=0 sb=0 sd=0 mult=1 m=1
XM8_3 bias21 bias21 VSS VSS sky130_fd_pr__nfet_01v8 L=1 W=1.25 nf=1 ad='int((nf+1)/2) * W/nf * 0.29'
+ as='int((nf+2)/2) * W/nf * 0.29' pd='2*int((nf+1)/2) * (W/nf + 0.29)' ps='2*int((nf+2)/2) * (W/nf + 0.29)'
+ nrd='0.29 / W' nrs='0.29 / W' sa=0 sb=0 sd=0 mult=1 m=1
XM100_4 IB IB VCC VCC sky130_fd_pr__pfet_01v8 L=3 W=5 nf=1 ad='int((nf+1)/2) * W/nf * 0.29' as='int((nf+2)/2) * W/nf * 0.29'
+ pd='2*int((nf+1)/2) * (W/nf + 0.29)' ps='2*int((nf+2)/2) * (W/nf + 0.29)' nrd='0.29 / W' nrs='0.29 / W'
+ sa=0 sb=0 sd=0 mult=2 m=2
XM3_dummy_1 dummy_3 VB_B dummy_3 VSS sky130_fd_pr__nfet_01v8 L=5 W=5 nf=1 ad='int((nf+1)/2) * W/nf * 0.29'
+ as='int((nf+2)/2) * W/nf * 0.29' pd='2*int((nf+1)/2) * (W/nf + 0.29)' ps='2*int((nf+2)/2) * (W/nf + 0.29)'
+ nrd='0.29 / W' nrs='0.29 / W' sa=0 sb=0 sd=0 mult=17 m=17
XM3_dummy_2 dummy_3 VB_B dummy_3 VSS sky130_fd_pr__nfet_01v8 L=5 W=5 nf=1 ad='int((nf+1)/2) * W/nf * 0.29'
+ as='int((nf+2)/2) * W/nf * 0.29' pd='2*int((nf+1)/2) * (W/nf + 0.29)' ps='2*int((nf+2)/2) * (W/nf + 0.29)'
+ nrd='0.29 / W' nrs='0.29 / W' sa=0 sb=0 sd=0 mult=17 m=17
XM3_dummy_3 dummy_3 VB_B dummy_3 VSS sky130_fd_pr__nfet_01v8 L=5 W=5 nf=1 ad='int((nf+1)/2) * W/nf * 0.29'
+ as='int((nf+2)/2) * W/nf * 0.29' pd='2*int((nf+1)/2) * (W/nf + 0.29)' ps='2*int((nf+2)/2) * (W/nf + 0.29)'
+ nrd='0.29 / W' nrs='0.29 / W' sa=0 sb=0 sd=0 mult=1 m=1
XM3_dummy_4 dummy_3 VB_B dummy_3 VSS sky130_fd_pr__nfet_01v8 L=5 W=5 nf=1 ad='int((nf+1)/2) * W/nf * 0.29'
+ as='int((nf+2)/2) * W/nf * 0.29' pd='2*int((nf+1)/2) * (W/nf + 0.29)' ps='2*int((nf+2)/2) * (W/nf + 0.29)'
+ nrd='0.29 / W' nrs='0.29 / W' sa=0 sb=0 sd=0 mult=1 m=1
XM3_dummy_5 dummy_3 VB_B dummy_3 VSS sky130_fd_pr__nfet_01v8 L=5 W=5 nf=1 ad='int((nf+1)/2) * W/nf * 0.29'
+ as='int((nf+2)/2) * W/nf * 0.29' pd='2*int((nf+1)/2) * (W/nf + 0.29)' ps='2*int((nf+2)/2) * (W/nf + 0.29)'
+ nrd='0.29 / W' nrs='0.29 / W' sa=0 sb=0 sd=0 mult=1 m=1
XM3_dummy_6 dummy_3 VB_B dummy_3 VSS sky130_fd_pr__nfet_01v8 L=5 W=5 nf=1 ad='int((nf+1)/2) * W/nf * 0.29'
+ as='int((nf+2)/2) * W/nf * 0.29' pd='2*int((nf+1)/2) * (W/nf + 0.29)' ps='2*int((nf+2)/2) * (W/nf + 0.29)'
+ nrd='0.29 / W' nrs='0.29 / W' sa=0 sb=0 sd=0 mult=1 m=1
XM3_dummy_7 dummy_3 VB_B dummy_3 VSS sky130_fd_pr__nfet_01v8 L=5 W=5 nf=1 ad='int((nf+1)/2) * W/nf * 0.29'
+ as='int((nf+2)/2) * W/nf * 0.29' pd='2*int((nf+1)/2) * (W/nf + 0.29)' ps='2*int((nf+2)/2) * (W/nf + 0.29)'
+ nrd='0.29 / W' nrs='0.29 / W' sa=0 sb=0 sd=0 mult=1 m=1
XM3_dummy_8 dummy_3 VB_B dummy_3 VSS sky130_fd_pr__nfet_01v8 L=5 W=5 nf=1 ad='int((nf+1)/2) * W/nf * 0.29'
+ as='int((nf+2)/2) * W/nf * 0.29' pd='2*int((nf+1)/2) * (W/nf + 0.29)' ps='2*int((nf+2)/2) * (W/nf + 0.29)'
+ nrd='0.29 / W' nrs='0.29 / W' sa=0 sb=0 sd=0 mult=1 m=1
XM3_dummy_9 dummy_3 VB_B dummy_3 VSS sky130_fd_pr__nfet_01v8 L=5 W=5 nf=1 ad='int((nf+1)/2) * W/nf * 0.29'
+ as='int((nf+2)/2) * W/nf * 0.29' pd='2*int((nf+1)/2) * (W/nf + 0.29)' ps='2*int((nf+2)/2) * (W/nf + 0.29)'
+ nrd='0.29 / W' nrs='0.29 / W' sa=0 sb=0 sd=0 mult=1 m=1
XM3_dummy_10 dummy_3 VB_B dummy_3 VSS sky130_fd_pr__nfet_01v8 L=5 W=5 nf=1 ad='int((nf+1)/2) * W/nf * 0.29'
+ as='int((nf+2)/2) * W/nf * 0.29' pd='2*int((nf+1)/2) * (W/nf + 0.29)' ps='2*int((nf+2)/2) * (W/nf + 0.29)'
+ nrd='0.29 / W' nrs='0.29 / W' sa=0 sb=0 sd=0 mult=1 m=1
XM9_dummy_13 dummy_9 bias1 dummy_9 VCC sky130_fd_pr__pfet_01v8 L=15 W=5 nf=1 ad='int((nf+1)/2) * W/nf * 0.29'
+ as='int((nf+2)/2) * W/nf * 0.29' pd='2*int((nf+1)/2) * (W/nf + 0.29)' ps='2*int((nf+2)/2) * (W/nf + 0.29)'
+ nrd='0.29 / W' nrs='0.29 / W' sa=0 sb=0 sd=0 mult=1 m=1
XM9_dummy_14 dummy_9 bias1 dummy_9 VCC sky130_fd_pr__pfet_01v8 L=15 W=5 nf=1 ad='int((nf+1)/2) * W/nf * 0.29'
+ as='int((nf+2)/2) * W/nf * 0.29' pd='2*int((nf+1)/2) * (W/nf + 0.29)' ps='2*int((nf+2)/2) * (W/nf + 0.29)'
+ nrd='0.29 / W' nrs='0.29 / W' sa=0 sb=0 sd=0 mult=1 m=1
XM9_dummy_15 dummy_9 bias1 dummy_9 VCC sky130_fd_pr__pfet_01v8 L=15 W=5 nf=1 ad='int((nf+1)/2) * W/nf * 0.29'
+ as='int((nf+2)/2) * W/nf * 0.29' pd='2*int((nf+1)/2) * (W/nf + 0.29)' ps='2*int((nf+2)/2) * (W/nf + 0.29)'
+ nrd='0.29 / W' nrs='0.29 / W' sa=0 sb=0 sd=0 mult=1 m=1
XM9_dummy_16 dummy_9 bias1 dummy_9 VCC sky130_fd_pr__pfet_01v8 L=15 W=5 nf=1 ad='int((nf+1)/2) * W/nf * 0.29'
+ as='int((nf+2)/2) * W/nf * 0.29' pd='2*int((nf+1)/2) * (W/nf + 0.29)' ps='2*int((nf+2)/2) * (W/nf + 0.29)'
+ nrd='0.29 / W' nrs='0.29 / W' sa=0 sb=0 sd=0 mult=1 m=1
XM9_dummy_17 dummy_9 bias1 dummy_9 VCC sky130_fd_pr__pfet_01v8 L=15 W=5 nf=1 ad='int((nf+1)/2) * W/nf * 0.29'
+ as='int((nf+2)/2) * W/nf * 0.29' pd='2*int((nf+1)/2) * (W/nf + 0.29)' ps='2*int((nf+2)/2) * (W/nf + 0.29)'
+ nrd='0.29 / W' nrs='0.29 / W' sa=0 sb=0 sd=0 mult=1 m=1
XM9_dummy_18 dummy_9 bias1 dummy_9 VCC sky130_fd_pr__pfet_01v8 L=15 W=5 nf=1 ad='int((nf+1)/2) * W/nf * 0.29'
+ as='int((nf+2)/2) * W/nf * 0.29' pd='2*int((nf+1)/2) * (W/nf + 0.29)' ps='2*int((nf+2)/2) * (W/nf + 0.29)'
+ nrd='0.29 / W' nrs='0.29 / W' sa=0 sb=0 sd=0 mult=1 m=1
XM9_dummy_19 dummy_9 bias1 dummy_9 VCC sky130_fd_pr__pfet_01v8 L=15 W=5 nf=1 ad='int((nf+1)/2) * W/nf * 0.29'
+ as='int((nf+2)/2) * W/nf * 0.29' pd='2*int((nf+1)/2) * (W/nf + 0.29)' ps='2*int((nf+2)/2) * (W/nf + 0.29)'
+ nrd='0.29 / W' nrs='0.29 / W' sa=0 sb=0 sd=0 mult=1 m=1
XM9_dummy_20 dummy_9 bias1 dummy_9 VCC sky130_fd_pr__pfet_01v8 L=15 W=5 nf=1 ad='int((nf+1)/2) * W/nf * 0.29'
+ as='int((nf+2)/2) * W/nf * 0.29' pd='2*int((nf+1)/2) * (W/nf + 0.29)' ps='2*int((nf+2)/2) * (W/nf + 0.29)'
+ nrd='0.29 / W' nrs='0.29 / W' sa=0 sb=0 sd=0 mult=1 m=1
XM9_dummy_21 dummy_9 bias1 dummy_9 VCC sky130_fd_pr__pfet_01v8 L=15 W=5 nf=1 ad='int((nf+1)/2) * W/nf * 0.29'
+ as='int((nf+2)/2) * W/nf * 0.29' pd='2*int((nf+1)/2) * (W/nf + 0.29)' ps='2*int((nf+2)/2) * (W/nf + 0.29)'
+ nrd='0.29 / W' nrs='0.29 / W' sa=0 sb=0 sd=0 mult=1 m=1
XM9_dummy_22 dummy_9 bias1 dummy_9 VCC sky130_fd_pr__pfet_01v8 L=15 W=5 nf=1 ad='int((nf+1)/2) * W/nf * 0.29'
+ as='int((nf+2)/2) * W/nf * 0.29' pd='2*int((nf+1)/2) * (W/nf + 0.29)' ps='2*int((nf+2)/2) * (W/nf + 0.29)'
+ nrd='0.29 / W' nrs='0.29 / W' sa=0 sb=0 sd=0 mult=1 m=1
.ends

.GLOBAL GND
.end
